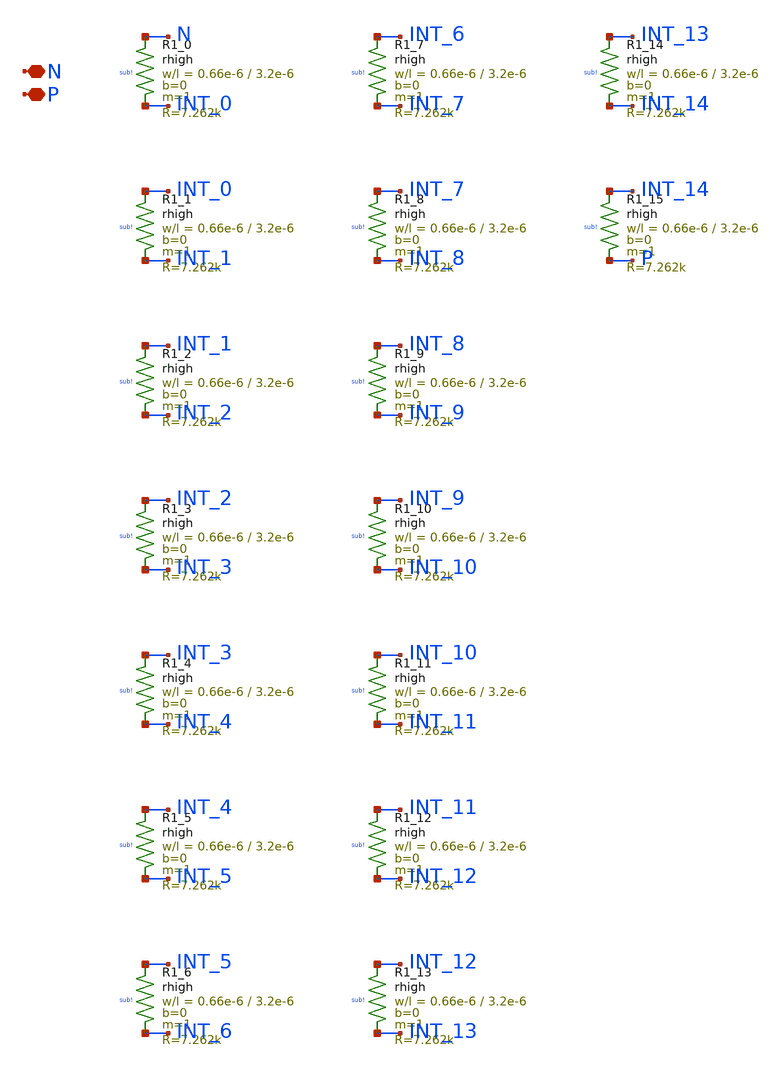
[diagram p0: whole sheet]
** sch_path: design/LELO_TR_IHP13G2/LELOTR_RES16.sch
**.subckt LELOTR_RES16 N P
*.iopin N
*.iopin P
XR1_0 N INT_0 sub! rhigh w=0.66e-6 l=3.2e-6 m=1 b=0 mm_ok=1
XR1_1 INT_0 INT_1 sub! rhigh w=0.66e-6 l=3.2e-6 m=1 b=0 mm_ok=1
XR1_2 INT_1 INT_2 sub! rhigh w=0.66e-6 l=3.2e-6 m=1 b=0 mm_ok=1
XR1_3 INT_2 INT_3 sub! rhigh w=0.66e-6 l=3.2e-6 m=1 b=0 mm_ok=1
XR1_4 INT_3 INT_4 sub! rhigh w=0.66e-6 l=3.2e-6 m=1 b=0 mm_ok=1
XR1_5 INT_4 INT_5 sub! rhigh w=0.66e-6 l=3.2e-6 m=1 b=0 mm_ok=1
XR1_6 INT_5 INT_6 sub! rhigh w=0.66e-6 l=3.2e-6 m=1 b=0 mm_ok=1
XR1_7 INT_6 INT_7 sub! rhigh w=0.66e-6 l=3.2e-6 m=1 b=0 mm_ok=1
XR1_8 INT_7 INT_8 sub! rhigh w=0.66e-6 l=3.2e-6 m=1 b=0 mm_ok=1
XR1_9 INT_8 INT_9 sub! rhigh w=0.66e-6 l=3.2e-6 m=1 b=0 mm_ok=1
XR1_10 INT_9 INT_10 sub! rhigh w=0.66e-6 l=3.2e-6 m=1 b=0 mm_ok=1
XR1_11 INT_10 INT_11 sub! rhigh w=0.66e-6 l=3.2e-6 m=1 b=0 mm_ok=1
XR1_12 INT_11 INT_12 sub! rhigh w=0.66e-6 l=3.2e-6 m=1 b=0 mm_ok=1
XR1_13 INT_12 INT_13 sub! rhigh w=0.66e-6 l=3.2e-6 m=1 b=0 mm_ok=1
XR1_14 INT_13 INT_14 sub! rhigh w=0.66e-6 l=3.2e-6 m=1 b=0 mm_ok=1
XR1_15 INT_14 P sub! rhigh w=0.66e-6 l=3.2e-6 m=1 b=0 mm_ok=1
**.ends
.end
